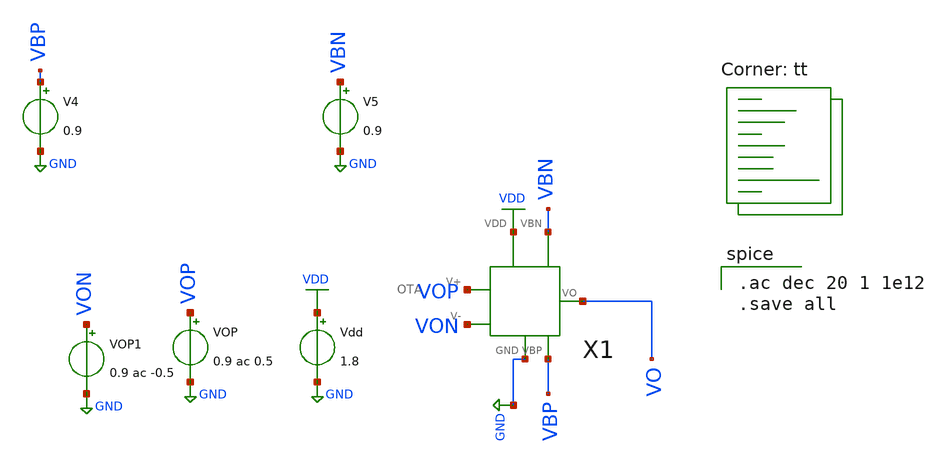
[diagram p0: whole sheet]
** sch_path: pll/pfd_cp_lf_lib/CP/xschem/untitled-2.sch
**.subckt untitled-2
X1 VOP VO VON VDD GND VBN VBP OTA
Vdd VDD GND 1.8
VOP VOP GND 0.9 ac 0.5
VOP1 VON GND 0.9 ac -0.5
V4 VBP GND 0.9
V5 VBN GND 0.9
**** begin user architecture code
.lib $::SKYWATER_MODELS/sky130.lib.spice tt

.ac dec 20 1 1e12
.save all

**** end user architecture code
**.ends

* expanding   symbol:  OTA.sym # of pins=7
** sym_path: pll/pfd_cp_lf_lib/CP/xschem/OTA.sym
** sch_path: pll/pfd_cp_lf_lib/CP/xschem/OTA.sch
.subckt OTA V+ VO V- VDD GND VBN VBP
*.ipin V+
*.ipin V-
*.opin VO
*.iopin VDD
*.iopin GND
*.ipin VBN
*.ipin VBP
XM9 P_bias N_bias GND GND sky130_fd_pr__nfet_01v8 L=0.6 W=2 nf=1 ad='int((nf+1)/2) * W/nf * 0.29' as='int((nf+2)/2) * W/nf * 0.29'
+ pd='2*int((nf+1)/2) * (W/nf + 0.29)' ps='2*int((nf+2)/2) * (W/nf + 0.29)' nrd='0.29 / W' nrs='0.29 / W'
+ sa=0 sb=0 sd=0 mult=2 m=2
XM10 N_bias N_bias GND GND sky130_fd_pr__nfet_01v8 L=0.6 W=2 nf=1 ad='int((nf+1)/2) * W/nf * 0.29' as='int((nf+2)/2) * W/nf * 0.29'
+ pd='2*int((nf+1)/2) * (W/nf + 0.29)' ps='2*int((nf+2)/2) * (W/nf + 0.29)' nrd='0.29 / W' nrs='0.29 / W'
+ sa=0 sb=0 sd=0 mult=1 m=1
XM16 P_bias P_bias VDD VDD sky130_fd_pr__pfet_01v8 L=0.6 W=6.66 nf=1 ad='int((nf+1)/2) * W/nf * 0.29'
+ as='int((nf+2)/2) * W/nf * 0.29' pd='2*int((nf+1)/2) * (W/nf + 0.29)' ps='2*int((nf+2)/2) * (W/nf + 0.29)'
+ nrd='0.29 / W' nrs='0.29 / W' sa=0 sb=0 sd=0 mult=2 m=2
I0 VDD N_bias 10u
XM13 net2 N_bias GND GND sky130_fd_pr__nfet_01v8 L=0.6 W=2 nf=1 ad='int((nf+1)/2) * W/nf * 0.29' as='int((nf+2)/2) * W/nf * 0.29'
+ pd='2*int((nf+1)/2) * (W/nf + 0.29)' ps='2*int((nf+2)/2) * (W/nf + 0.29)' nrd='0.29 / W' nrs='0.29 / W'
+ sa=0 sb=0 sd=0 mult=3 m=3
XM7 net1 P_bias VDD VDD sky130_fd_pr__pfet_01v8 L=0.6 W=6.66 nf=1 ad='int((nf+1)/2) * W/nf * 0.29' as='int((nf+2)/2) * W/nf * 0.29'
+ pd='2*int((nf+1)/2) * (W/nf + 0.29)' ps='2*int((nf+2)/2) * (W/nf + 0.29)' nrd='0.29 / W' nrs='0.29 / W'
+ sa=0 sb=0 sd=0 mult=2 m=2
XM8 net3 P_bias VDD VDD sky130_fd_pr__pfet_01v8 L=0.6 W=6.66 nf=1 ad='int((nf+1)/2) * W/nf * 0.29' as='int((nf+2)/2) * W/nf * 0.29'
+ pd='2*int((nf+1)/2) * (W/nf + 0.29)' ps='2*int((nf+2)/2) * (W/nf + 0.29)' nrd='0.29 / W' nrs='0.29 / W'
+ sa=0 sb=0 sd=0 mult=2 m=2
XM11 net3 V- net2 GND sky130_fd_pr__nfet_01v8 L=0.15 W=1 nf=1 ad='int((nf+1)/2) * W/nf * 0.29' as='int((nf+2)/2) * W/nf * 0.29'
+ pd='2*int((nf+1)/2) * (W/nf + 0.29)' ps='2*int((nf+2)/2) * (W/nf + 0.29)' nrd='0.29 / W' nrs='0.29 / W'
+ sa=0 sb=0 sd=0 mult=1 m=1
XM12 net1 V+ net2 GND sky130_fd_pr__nfet_01v8 L=0.15 W=1 nf=1 ad='int((nf+1)/2) * W/nf * 0.29' as='int((nf+2)/2) * W/nf * 0.29'
+ pd='2*int((nf+1)/2) * (W/nf + 0.29)' ps='2*int((nf+2)/2) * (W/nf + 0.29)' nrd='0.29 / W' nrs='0.29 / W'
+ sa=0 sb=0 sd=0 mult=1 m=1
XM1 net5 net4 GND GND sky130_fd_pr__nfet_01v8 L=0.15 W=1 nf=1 ad='int((nf+1)/2) * W/nf * 0.29' as='int((nf+2)/2) * W/nf * 0.29'
+ pd='2*int((nf+1)/2) * (W/nf + 0.29)' ps='2*int((nf+2)/2) * (W/nf + 0.29)' nrd='0.29 / W' nrs='0.29 / W'
+ sa=0 sb=0 sd=0 mult=1 m=1
XM2 GND net4 GND GND sky130_fd_pr__nfet_01v8 L=0.15 W=1 nf=1 ad='int((nf+1)/2) * W/nf * 0.29' as='int((nf+2)/2) * W/nf * 0.29'
+ pd='2*int((nf+1)/2) * (W/nf + 0.29)' ps='2*int((nf+2)/2) * (W/nf + 0.29)' nrd='0.29 / W' nrs='0.29 / W'
+ sa=0 sb=0 sd=0 mult=1 m=1
XM3 net4 VBN net5 GND sky130_fd_pr__nfet_01v8 L=0.15 W=1 nf=1 ad='int((nf+1)/2) * W/nf * 0.29' as='int((nf+2)/2) * W/nf * 0.29'
+ pd='2*int((nf+1)/2) * (W/nf + 0.29)' ps='2*int((nf+2)/2) * (W/nf + 0.29)' nrd='0.29 / W' nrs='0.29 / W'
+ sa=0 sb=0 sd=0 mult=1 m=1
XM4 VO VBN GND GND sky130_fd_pr__nfet_01v8 L=0.15 W=1 nf=1 ad='int((nf+1)/2) * W/nf * 0.29' as='int((nf+2)/2) * W/nf * 0.29'
+ pd='2*int((nf+1)/2) * (W/nf + 0.29)' ps='2*int((nf+2)/2) * (W/nf + 0.29)' nrd='0.29 / W' nrs='0.29 / W'
+ sa=0 sb=0 sd=0 mult=1 m=1
XM5 VO VBP net3 VDD sky130_fd_pr__pfet_01v8 L=0.15 W=1 nf=1 ad='int((nf+1)/2) * W/nf * 0.29' as='int((nf+2)/2) * W/nf * 0.29'
+ pd='2*int((nf+1)/2) * (W/nf + 0.29)' ps='2*int((nf+2)/2) * (W/nf + 0.29)' nrd='0.29 / W' nrs='0.29 / W'
+ sa=0 sb=0 sd=0 mult=1 m=1
XM6 net4 VBP net1 VDD sky130_fd_pr__pfet_01v8 L=0.15 W=1 nf=1 ad='int((nf+1)/2) * W/nf * 0.29' as='int((nf+2)/2) * W/nf * 0.29'
+ pd='2*int((nf+1)/2) * (W/nf + 0.29)' ps='2*int((nf+2)/2) * (W/nf + 0.29)' nrd='0.29 / W' nrs='0.29 / W'
+ sa=0 sb=0 sd=0 mult=1 m=1
XM18 net6 P_bias VDD VDD sky130_fd_pr__pfet_01v8 L=0.6 W=6.66 nf=1 ad='int((nf+1)/2) * W/nf * 0.29' as='int((nf+2)/2) * W/nf * 0.29'
+ pd='2*int((nf+1)/2) * (W/nf + 0.29)' ps='2*int((nf+2)/2) * (W/nf + 0.29)' nrd='0.29 / W' nrs='0.29 / W'
+ sa=0 sb=0 sd=0 mult=2 m=2
XM14 GND V- net6 VDD sky130_fd_pr__pfet_01v8 L=0.15 W=1 nf=1 ad='int((nf+1)/2) * W/nf * 0.29' as='int((nf+2)/2) * W/nf * 0.29'
+ pd='2*int((nf+1)/2) * (W/nf + 0.29)' ps='2*int((nf+2)/2) * (W/nf + 0.29)' nrd='0.29 / W' nrs='0.29 / W'
+ sa=0 sb=0 sd=0 mult=1 m=1
XM15 net5 V+ net6 VDD sky130_fd_pr__pfet_01v8 L=0.15 W=1 nf=1 ad='int((nf+1)/2) * W/nf * 0.29' as='int((nf+2)/2) * W/nf * 0.29'
+ pd='2*int((nf+1)/2) * (W/nf + 0.29)' ps='2*int((nf+2)/2) * (W/nf + 0.29)' nrd='0.29 / W' nrs='0.29 / W'
+ sa=0 sb=0 sd=0 mult=1 m=1
.ends

.GLOBAL GND
.GLOBAL VDD
.end
